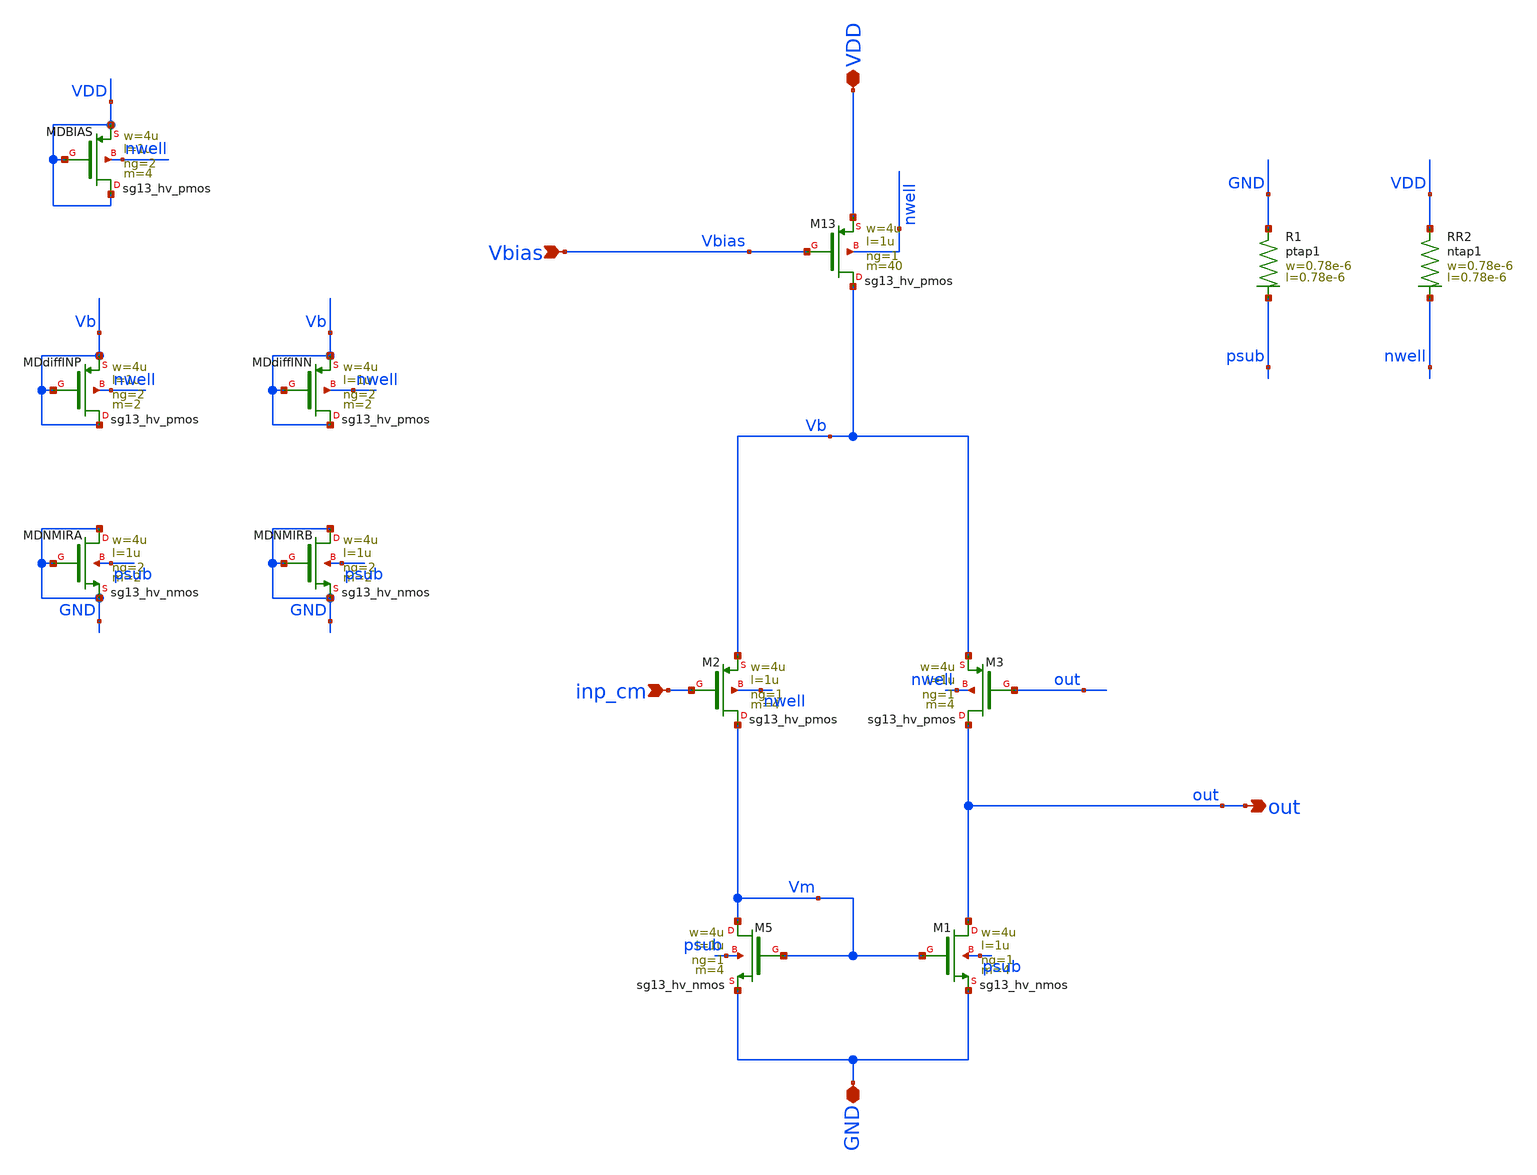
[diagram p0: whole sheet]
** sch_path: xschem/buffer_final.sch
**.subckt buffer_final inp_cm out VDD GND Vbias
*.ipin inp_cm
*.opin out
*.iopin VDD
*.iopin GND
*.ipin Vbias
XM2 Vm inp_cm Vb nwell sg13_hv_pmos w=4u l=1u ng=1 m=4 mm_ok=1
XM5 Vm Vm GND psub sg13_hv_nmos w=4u l=1u ng=1 m=4 mm_ok=1
XM13 Vb Vbias VDD nwell sg13_hv_pmos w=4u l=1u ng=1 m=40 mm_ok=1
XM3 out out Vb nwell sg13_hv_pmos w=4u l=1u ng=1 m=4 mm_ok=1
XM1 out Vm GND psub sg13_hv_nmos w=4u l=1u ng=1 m=4 mm_ok=1
XR1 GND psub ptap1 R=262.8 w=0.78e-6 l=0.78e-6
XR2 VDD nwell ntap1 R=262.8 w=0.78e-6 l=0.78e-6
XMDBIAS VDD VDD VDD nwell sg13_hv_pmos w=4u l=1u ng=2 m=4 mm_ok=1
XMDdiffINP Vb Vb Vb nwell sg13_hv_pmos w=4u l=1u ng=2 m=2 mm_ok=1
XMDdiffINN Vb Vb Vb nwell sg13_hv_pmos w=4u l=1u ng=2 m=2 mm_ok=1
XMDNMIRA GND GND GND psub sg13_hv_nmos w=4u l=1u ng=2 m=2 mm_ok=1
XMDNMIRB GND GND GND psub sg13_hv_nmos w=4u l=1u ng=2 m=2 mm_ok=1
**.ends
.end
